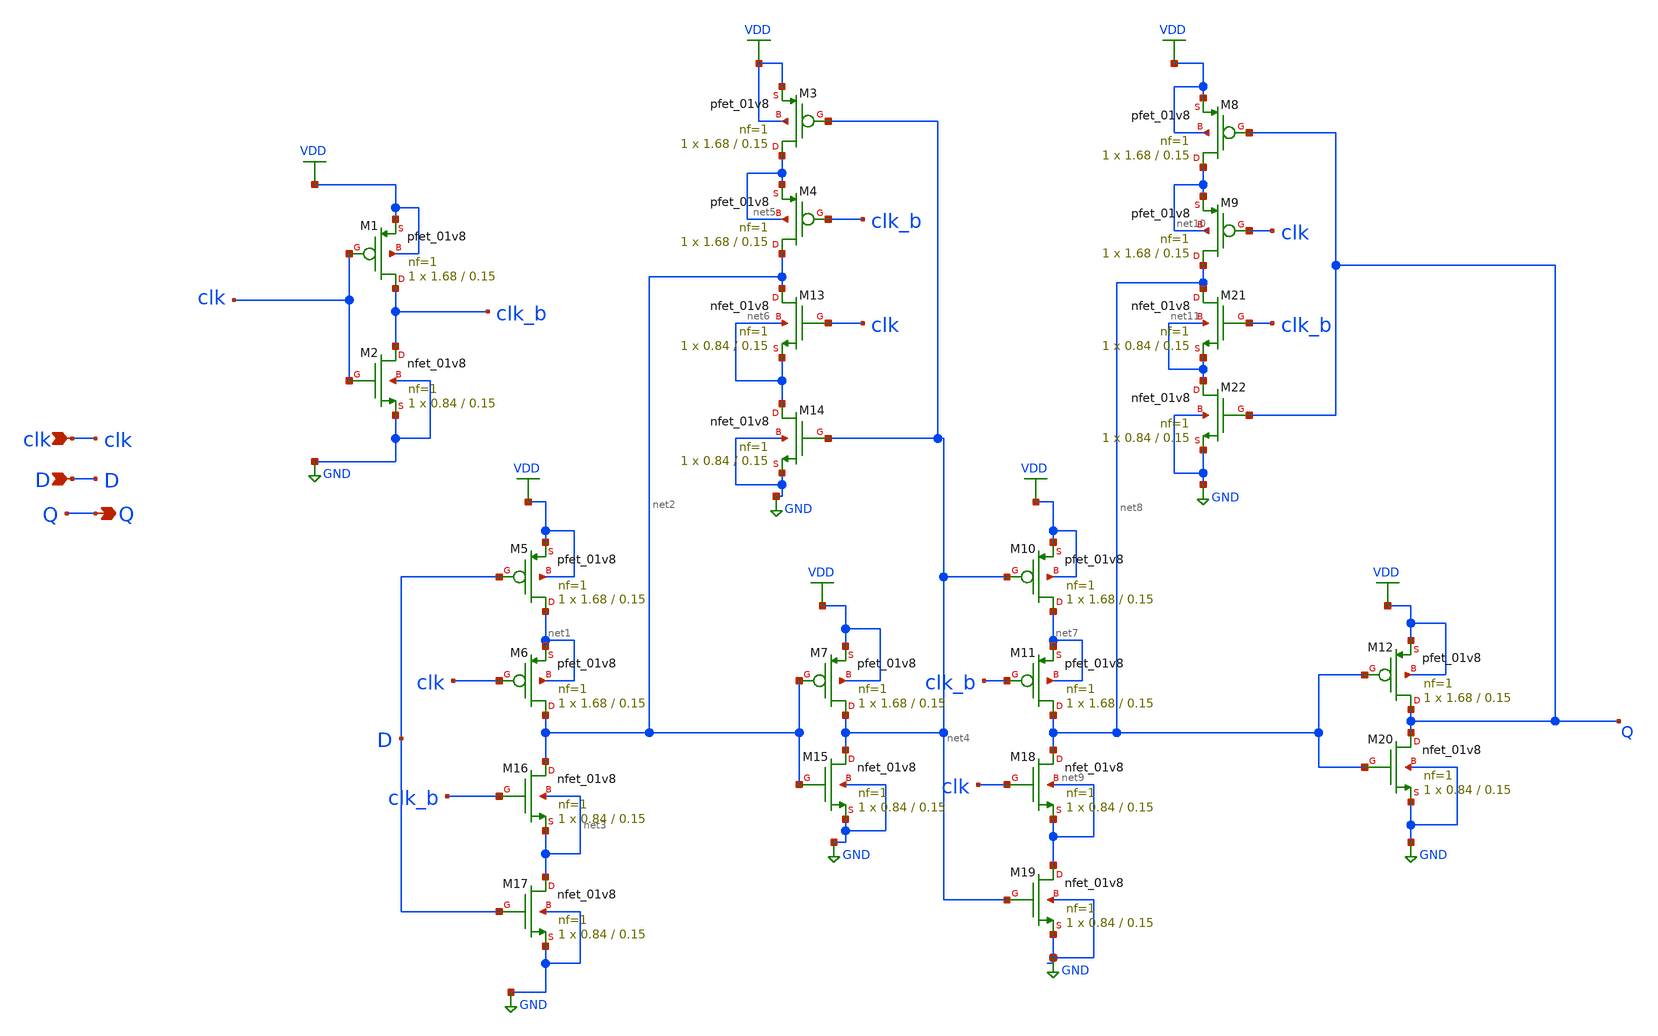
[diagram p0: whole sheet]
** sch_path: xschem/dflipflop.sch
**.subckt dflipflop clk D Q
*.ipin clk
*.ipin D
*.opin Q
XM1 clk_b clk VDD VDD sky130_fd_pr__pfet_01v8 L=0.15 W=1.68 nf=1 ad='int((nf+1)/2) * W/nf * 0.29' as='int((nf+2)/2) * W/nf * 0.29'
+ pd='2*int((nf+1)/2) * (W/nf + 0.29)' ps='2*int((nf+2)/2) * (W/nf + 0.29)' nrd='0.29 / W' nrs='0.29 / W'
+ sa=0 sb=0 sd=0 mult=1 m=1
XM2 clk_b clk GND GND sky130_fd_pr__nfet_01v8 L=0.15 W=0.84 nf=1 ad='int((nf+1)/2) * W/nf * 0.29' as='int((nf+2)/2) * W/nf * 0.29'
+ pd='2*int((nf+1)/2) * (W/nf + 0.29)' ps='2*int((nf+2)/2) * (W/nf + 0.29)' nrd='0.29 / W' nrs='0.29 / W'
+ sa=0 sb=0 sd=0 mult=1 m=1
XM3 net5 net4 VDD VDD sky130_fd_pr__pfet_01v8 L=0.15 W=1.68 nf=1 ad='int((nf+1)/2) * W/nf * 0.29' as='int((nf+2)/2) * W/nf * 0.29'
+ pd='2*int((nf+1)/2) * (W/nf + 0.29)' ps='2*int((nf+2)/2) * (W/nf + 0.29)' nrd='0.29 / W' nrs='0.29 / W'
+ sa=0 sb=0 sd=0 mult=1 m=1
XM4 net2 clk_b net5 net5 sky130_fd_pr__pfet_01v8 L=0.15 W=1.68 nf=1 ad='int((nf+1)/2) * W/nf * 0.29'
+ as='int((nf+2)/2) * W/nf * 0.29' pd='2*int((nf+1)/2) * (W/nf + 0.29)' ps='2*int((nf+2)/2) * (W/nf + 0.29)'
+ nrd='0.29 / W' nrs='0.29 / W' sa=0 sb=0 sd=0 mult=1 m=1
XM5 net1 D VDD VDD sky130_fd_pr__pfet_01v8 L=0.15 W=1.68 nf=1 ad='int((nf+1)/2) * W/nf * 0.29' as='int((nf+2)/2) * W/nf * 0.29'
+ pd='2*int((nf+1)/2) * (W/nf + 0.29)' ps='2*int((nf+2)/2) * (W/nf + 0.29)' nrd='0.29 / W' nrs='0.29 / W'
+ sa=0 sb=0 sd=0 mult=1 m=1
XM6 net2 clk net1 net1 sky130_fd_pr__pfet_01v8 L=0.15 W=1.68 nf=1 ad='int((nf+1)/2) * W/nf * 0.29' as='int((nf+2)/2) * W/nf * 0.29'
+ pd='2*int((nf+1)/2) * (W/nf + 0.29)' ps='2*int((nf+2)/2) * (W/nf + 0.29)' nrd='0.29 / W' nrs='0.29 / W'
+ sa=0 sb=0 sd=0 mult=1 m=1
XM7 net4 net2 VDD VDD sky130_fd_pr__pfet_01v8 L=0.15 W=1.68 nf=1 ad='int((nf+1)/2) * W/nf * 0.29' as='int((nf+2)/2) * W/nf * 0.29'
+ pd='2*int((nf+1)/2) * (W/nf + 0.29)' ps='2*int((nf+2)/2) * (W/nf + 0.29)' nrd='0.29 / W' nrs='0.29 / W'
+ sa=0 sb=0 sd=0 mult=1 m=1
XM8 net10 Q VDD VDD sky130_fd_pr__pfet_01v8 L=0.15 W=1.68 nf=1 ad='int((nf+1)/2) * W/nf * 0.29' as='int((nf+2)/2) * W/nf * 0.29'
+ pd='2*int((nf+1)/2) * (W/nf + 0.29)' ps='2*int((nf+2)/2) * (W/nf + 0.29)' nrd='0.29 / W' nrs='0.29 / W'
+ sa=0 sb=0 sd=0 mult=1 m=1
XM9 net8 clk net10 net10 sky130_fd_pr__pfet_01v8 L=0.15 W=1.68 nf=1 ad='int((nf+1)/2) * W/nf * 0.29'
+ as='int((nf+2)/2) * W/nf * 0.29' pd='2*int((nf+1)/2) * (W/nf + 0.29)' ps='2*int((nf+2)/2) * (W/nf + 0.29)'
+ nrd='0.29 / W' nrs='0.29 / W' sa=0 sb=0 sd=0 mult=1 m=1
XM10 net7 net4 VDD VDD sky130_fd_pr__pfet_01v8 L=0.15 W=1.68 nf=1 ad='int((nf+1)/2) * W/nf * 0.29' as='int((nf+2)/2) * W/nf * 0.29'
+ pd='2*int((nf+1)/2) * (W/nf + 0.29)' ps='2*int((nf+2)/2) * (W/nf + 0.29)' nrd='0.29 / W' nrs='0.29 / W'
+ sa=0 sb=0 sd=0 mult=1 m=1
XM11 net8 clk_b net7 net7 sky130_fd_pr__pfet_01v8 L=0.15 W=1.68 nf=1 ad='int((nf+1)/2) * W/nf * 0.29'
+ as='int((nf+2)/2) * W/nf * 0.29' pd='2*int((nf+1)/2) * (W/nf + 0.29)' ps='2*int((nf+2)/2) * (W/nf + 0.29)'
+ nrd='0.29 / W' nrs='0.29 / W' sa=0 sb=0 sd=0 mult=1 m=1
XM12 Q net8 VDD VDD sky130_fd_pr__pfet_01v8 L=0.15 W=1.68 nf=1 ad='int((nf+1)/2) * W/nf * 0.29' as='int((nf+2)/2) * W/nf * 0.29'
+ pd='2*int((nf+1)/2) * (W/nf + 0.29)' ps='2*int((nf+2)/2) * (W/nf + 0.29)' nrd='0.29 / W' nrs='0.29 / W'
+ sa=0 sb=0 sd=0 mult=1 m=1
XM13 net2 clk net6 net6 sky130_fd_pr__nfet_01v8 L=0.15 W=0.84 nf=1 ad='int((nf+1)/2) * W/nf * 0.29' as='int((nf+2)/2) * W/nf * 0.29'
+ pd='2*int((nf+1)/2) * (W/nf + 0.29)' ps='2*int((nf+2)/2) * (W/nf + 0.29)' nrd='0.29 / W' nrs='0.29 / W'
+ sa=0 sb=0 sd=0 mult=1 m=1
XM14 net6 net4 GND GND sky130_fd_pr__nfet_01v8 L=0.15 W=0.84 nf=1 ad='int((nf+1)/2) * W/nf * 0.29' as='int((nf+2)/2) * W/nf * 0.29'
+ pd='2*int((nf+1)/2) * (W/nf + 0.29)' ps='2*int((nf+2)/2) * (W/nf + 0.29)' nrd='0.29 / W' nrs='0.29 / W'
+ sa=0 sb=0 sd=0 mult=1 m=1
XM15 net4 net2 GND GND sky130_fd_pr__nfet_01v8 L=0.15 W=0.84 nf=1 ad='int((nf+1)/2) * W/nf * 0.29' as='int((nf+2)/2) * W/nf * 0.29'
+ pd='2*int((nf+1)/2) * (W/nf + 0.29)' ps='2*int((nf+2)/2) * (W/nf + 0.29)' nrd='0.29 / W' nrs='0.29 / W'
+ sa=0 sb=0 sd=0 mult=1 m=1
XM16 net2 clk_b net3 net3 sky130_fd_pr__nfet_01v8 L=0.15 W=0.84 nf=1 ad='int((nf+1)/2) * W/nf * 0.29'
+ as='int((nf+2)/2) * W/nf * 0.29' pd='2*int((nf+1)/2) * (W/nf + 0.29)' ps='2*int((nf+2)/2) * (W/nf + 0.29)'
+ nrd='0.29 / W' nrs='0.29 / W' sa=0 sb=0 sd=0 mult=1 m=1
XM17 net3 D GND GND sky130_fd_pr__nfet_01v8 L=0.15 W=0.84 nf=1 ad='int((nf+1)/2) * W/nf * 0.29' as='int((nf+2)/2) * W/nf * 0.29'
+ pd='2*int((nf+1)/2) * (W/nf + 0.29)' ps='2*int((nf+2)/2) * (W/nf + 0.29)' nrd='0.29 / W' nrs='0.29 / W'
+ sa=0 sb=0 sd=0 mult=1 m=1
XM18 net8 clk net9 net9 sky130_fd_pr__nfet_01v8 L=0.15 W=0.84 nf=1 ad='int((nf+1)/2) * W/nf * 0.29' as='int((nf+2)/2) * W/nf * 0.29'
+ pd='2*int((nf+1)/2) * (W/nf + 0.29)' ps='2*int((nf+2)/2) * (W/nf + 0.29)' nrd='0.29 / W' nrs='0.29 / W'
+ sa=0 sb=0 sd=0 mult=1 m=1
XM19 net9 net4 GND GND sky130_fd_pr__nfet_01v8 L=0.15 W=0.84 nf=1 ad='int((nf+1)/2) * W/nf * 0.29' as='int((nf+2)/2) * W/nf * 0.29'
+ pd='2*int((nf+1)/2) * (W/nf + 0.29)' ps='2*int((nf+2)/2) * (W/nf + 0.29)' nrd='0.29 / W' nrs='0.29 / W'
+ sa=0 sb=0 sd=0 mult=1 m=1
XM20 Q net8 GND GND sky130_fd_pr__nfet_01v8 L=0.15 W=0.84 nf=1 ad='int((nf+1)/2) * W/nf * 0.29' as='int((nf+2)/2) * W/nf * 0.29'
+ pd='2*int((nf+1)/2) * (W/nf + 0.29)' ps='2*int((nf+2)/2) * (W/nf + 0.29)' nrd='0.29 / W' nrs='0.29 / W'
+ sa=0 sb=0 sd=0 mult=1 m=1
XM21 net8 clk_b net11 net11 sky130_fd_pr__nfet_01v8 L=0.15 W=0.84 nf=1 ad='int((nf+1)/2) * W/nf * 0.29'
+ as='int((nf+2)/2) * W/nf * 0.29' pd='2*int((nf+1)/2) * (W/nf + 0.29)' ps='2*int((nf+2)/2) * (W/nf + 0.29)'
+ nrd='0.29 / W' nrs='0.29 / W' sa=0 sb=0 sd=0 mult=1 m=1
XM22 net11 Q GND GND sky130_fd_pr__nfet_01v8 L=0.15 W=0.84 nf=1 ad='int((nf+1)/2) * W/nf * 0.29' as='int((nf+2)/2) * W/nf * 0.29'
+ pd='2*int((nf+1)/2) * (W/nf + 0.29)' ps='2*int((nf+2)/2) * (W/nf + 0.29)' nrd='0.29 / W' nrs='0.29 / W'
+ sa=0 sb=0 sd=0 mult=1 m=1
**.ends
.GLOBAL GND
.GLOBAL VDD
.end
